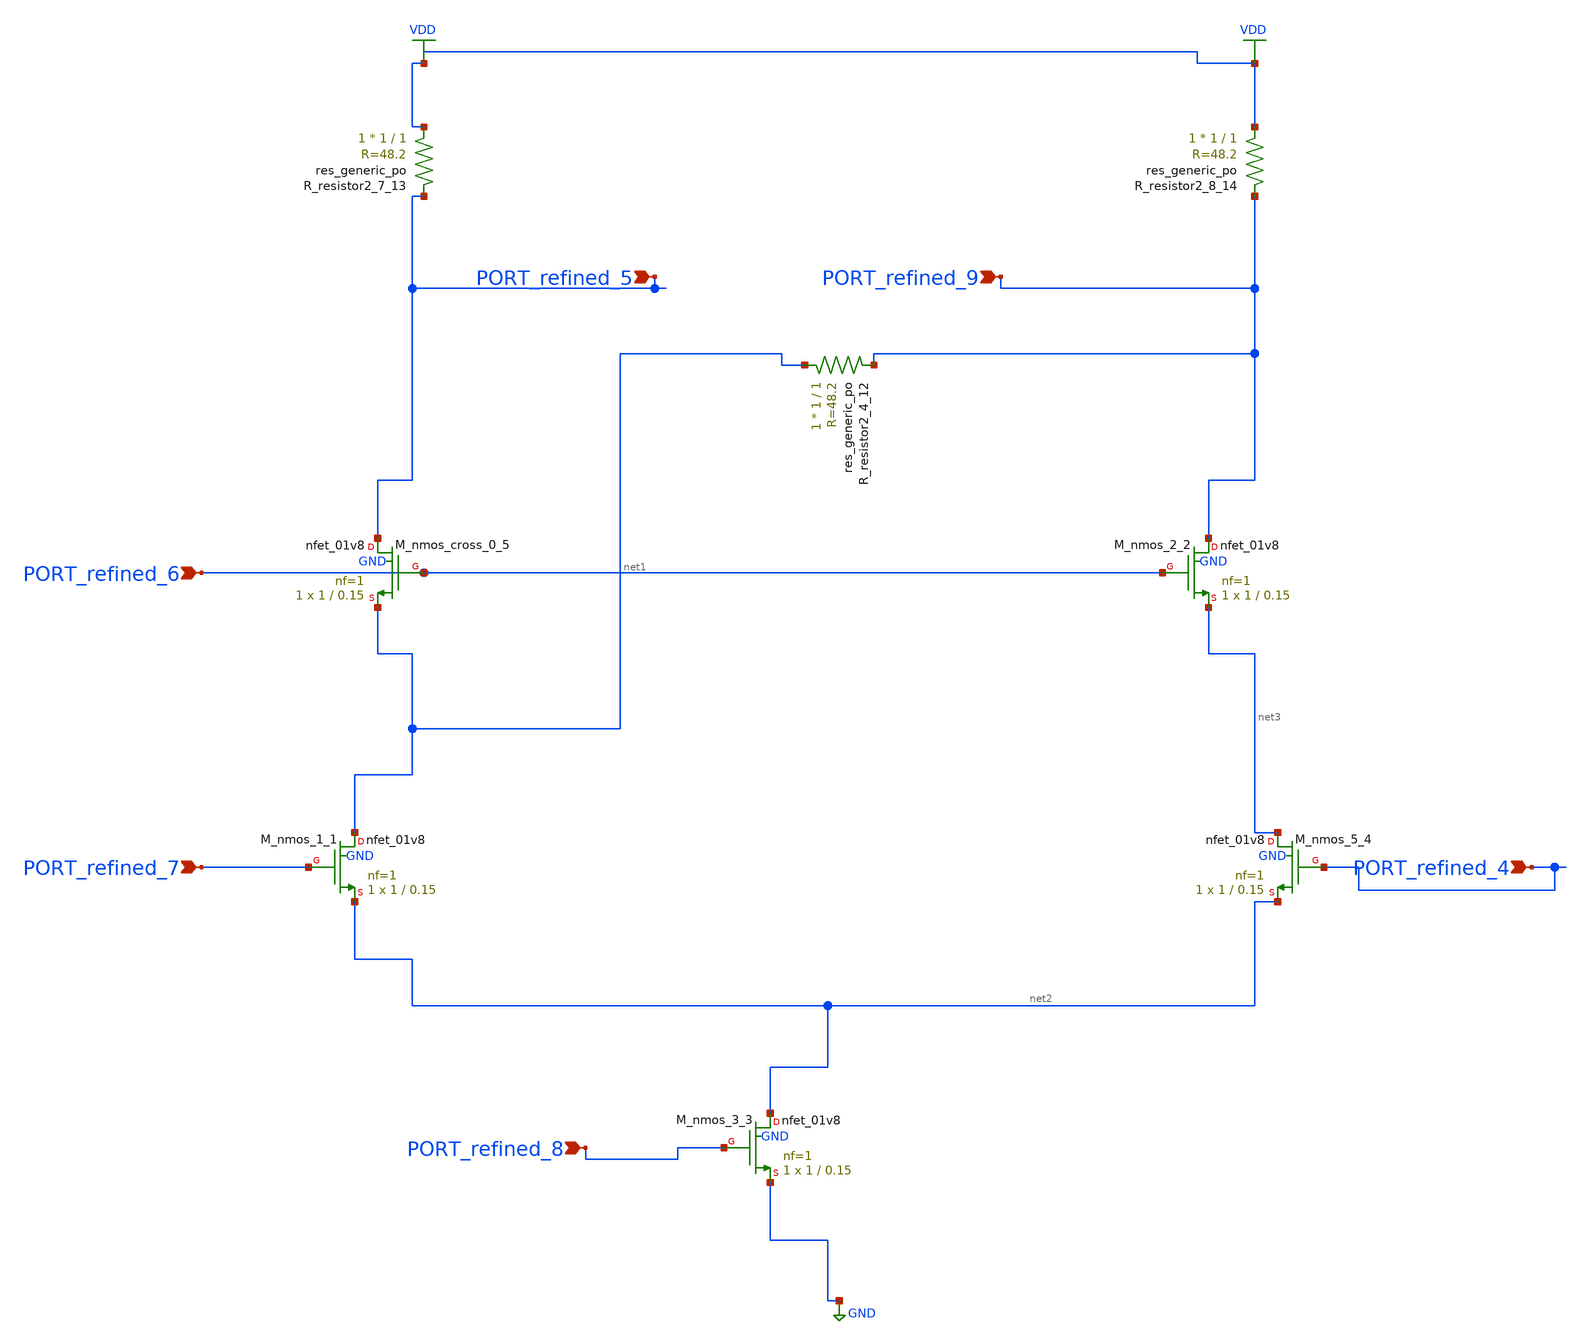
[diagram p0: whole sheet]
** sch_path: schematics/AMSNet/249.sch
**.subckt 249 PORT_refined_7 PORT_refined_8 PORT_refined_5 PORT_refined_9 PORT_refined_4
*+ PORT_refined_6
*.ipin PORT_refined_7
*.ipin PORT_refined_8
*.ipin PORT_refined_5
*.ipin PORT_refined_9
*.ipin PORT_refined_4
*.ipin PORT_refined_6
XM_nmos_1_1 net1 PORT_refined_7 net2 GND sky130_fd_pr__nfet_01v8 L=0.15 W=1 nf=1 ad='int((1 + 1)/2) * 1 / 1 * 0.29'
+ as='int((1 + 2)/2) * 1 / 1 * 0.29' pd='2*int((1 + 1)/2) * (1 / 1 + 0.29)' ps='2*int((1 + 2)/2) * (1 / 1 + 0.29)'
+ nrd='0.29 / 1 ' nrs='0.29 / 1 ' sa=0 sb=0 sd=0 mult=1 m=1
XM_nmos_2_2 PORT_refined_9 PORT_refined_6 net3 GND sky130_fd_pr__nfet_01v8 L=0.15 W=1 nf=1 ad='int((1 + 1)/2) * 1 / 1 * 0.29'
+ as='int((1 + 2)/2) * 1 / 1 * 0.29' pd='2*int((1 + 1)/2) * (1 / 1 + 0.29)' ps='2*int((1 + 2)/2) * (1 / 1 + 0.29)'
+ nrd='0.29 / 1 ' nrs='0.29 / 1 ' sa=0 sb=0 sd=0 mult=1 m=1
XM_nmos_3_3 net2 PORT_refined_8 GND GND sky130_fd_pr__nfet_01v8 L=0.15 W=1 nf=1 ad='int((1 + 1)/2) * 1 / 1 * 0.29'
+ as='int((1 + 2)/2) * 1 / 1 * 0.29' pd='2*int((1 + 1)/2) * (1 / 1 + 0.29)' ps='2*int((1 + 2)/2) * (1 / 1 + 0.29)'
+ nrd='0.29 / 1 ' nrs='0.29 / 1 ' sa=0 sb=0 sd=0 mult=1 m=1
XM_nmos_5_4 net3 PORT_refined_4 net2 GND sky130_fd_pr__nfet_01v8 L=0.15 W=1 nf=1 ad='int((1 + 1)/2) * 1 / 1 * 0.29'
+ as='int((1 + 2)/2) * 1 / 1 * 0.29' pd='2*int((1 + 1)/2) * (1 / 1 + 0.29)' ps='2*int((1 + 2)/2) * (1 / 1 + 0.29)'
+ nrd='0.29 / 1 ' nrs='0.29 / 1 ' sa=0 sb=0 sd=0 mult=1 m=1
XM_nmos_cross_0_5 PORT_refined_5 PORT_refined_6 net1 GND sky130_fd_pr__nfet_01v8 L=0.15 W=1 nf=1 ad='int((1 + 1)/2) * 1 / 1 * 0.29'
+ as='int((1 + 2)/2) * 1 / 1 * 0.29' pd='2*int((1 + 1)/2) * (1 / 1 + 0.29)' ps='2*int((1 + 2)/2) * (1 / 1 + 0.29)'
+ nrd='0.29 / 1 ' nrs='0.29 / 1 ' sa=0 sb=0 sd=0 mult=1 m=1
XR_resistor2_4_12 net1 PORT_refined_9 sky130_fd_pr__res_generic_po W=1 L=1 m=1
XR_resistor2_7_13 VDD PORT_refined_5 sky130_fd_pr__res_generic_po W=1 L=1 m=1
XR_resistor2_8_14 VDD PORT_refined_9 sky130_fd_pr__res_generic_po W=1 L=1 m=1
**.ends
.GLOBAL GND
.GLOBAL VDD
.end
